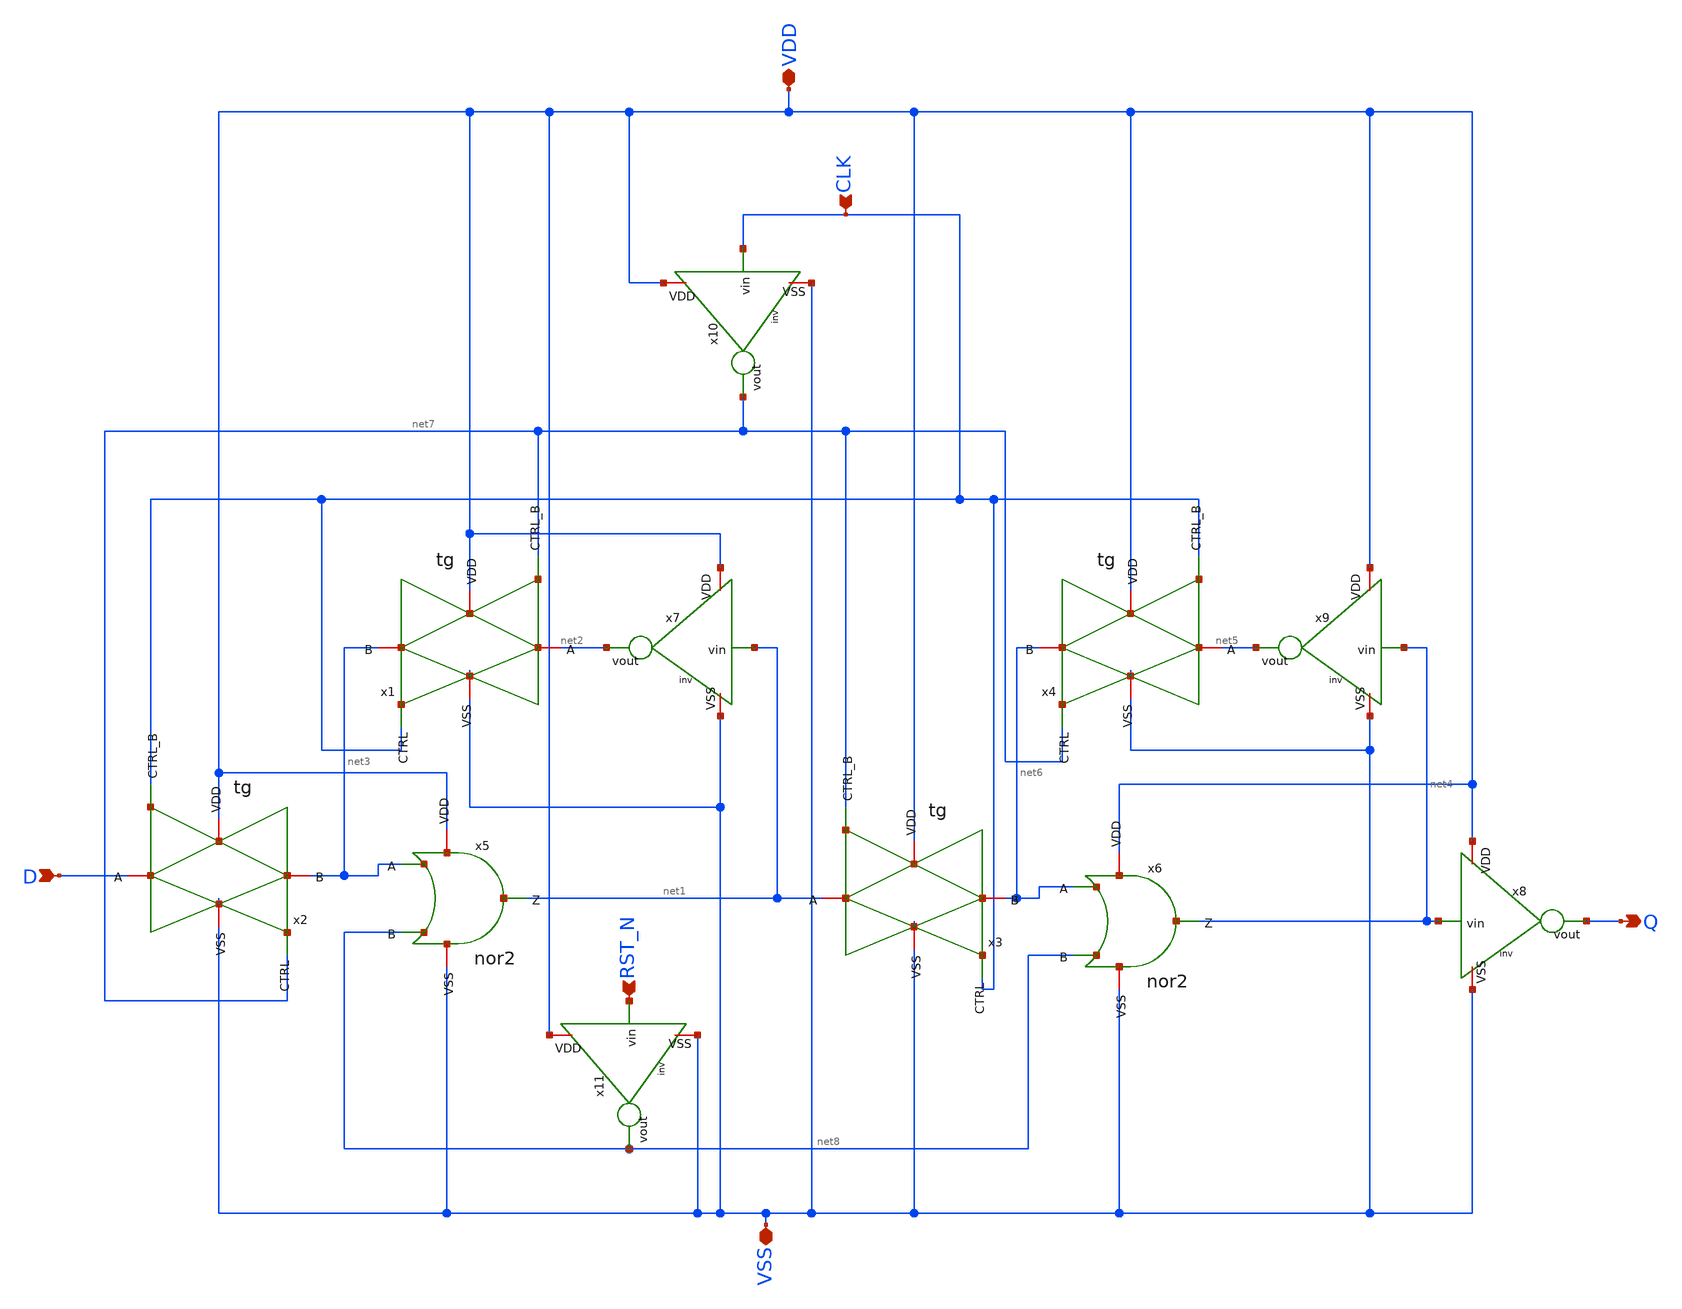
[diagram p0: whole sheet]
** sch_path: sar_logic/sar_designs/dff_set_n.sch
**.subckt dff_set_n D CLK RST_N Q VDD VSS
*.ipin D
*.ipin CLK
*.ipin RST_N
*.opin Q
*.iopin VDD
*.iopin VSS
x1 CLK VSS net2 net3 VDD net7 tg
x2 net7 VSS D net3 VDD CLK tg
x3 CLK VSS net1 net6 VDD net7 tg
x4 net7 VSS net5 net6 VDD CLK tg
x7 VDD net1 net2 VSS inv
x8 VDD net4 Q VSS inv
x9 VDD net4 net5 VSS inv
x10 VDD CLK net7 VSS inv
x5 VDD net3 net8 net1 VSS nor2
x6 VDD net6 net8 net4 VSS nor2
x11 VDD RST_N net8 VSS inv
**.ends
.end
